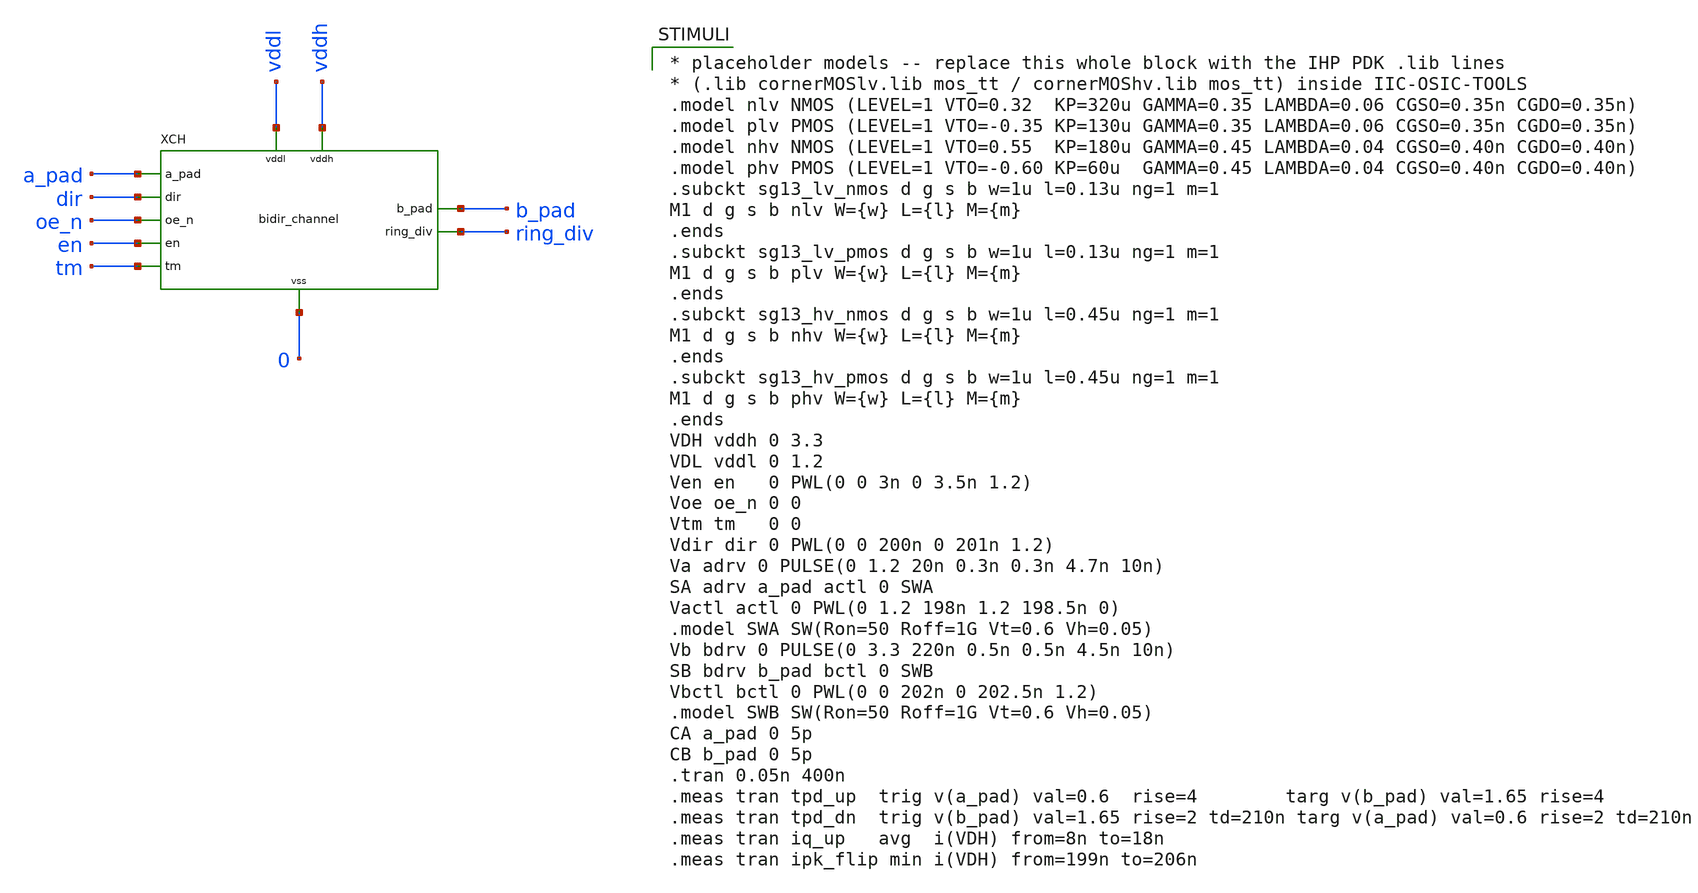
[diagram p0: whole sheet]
** sch_path: xschem/schematics/tb_bidir_channel.sch
**.subckt tb_bidir_channel
XCH a_pad b_pad dir oe_n en tm ring_div vddl vddh 0 bidir_channel
**** begin user architecture code

* placeholder models -- replace this whole block with the IHP PDK .lib lines
* (.lib cornerMOSlv.lib mos_tt / cornerMOShv.lib mos_tt) inside IIC-OSIC-TOOLS
.model nlv NMOS (LEVEL=1 VTO=0.32  KP=320u GAMMA=0.35 LAMBDA=0.06 CGSO=0.35n CGDO=0.35n)
.model plv PMOS (LEVEL=1 VTO=-0.35 KP=130u GAMMA=0.35 LAMBDA=0.06 CGSO=0.35n CGDO=0.35n)
.model nhv NMOS (LEVEL=1 VTO=0.55  KP=180u GAMMA=0.45 LAMBDA=0.04 CGSO=0.40n CGDO=0.40n)
.model phv PMOS (LEVEL=1 VTO=-0.60 KP=60u  GAMMA=0.45 LAMBDA=0.04 CGSO=0.40n CGDO=0.40n)
.subckt sg13_lv_nmos d g s b w=1u l=0.13u ng=1 m=1
M1 d g s b nlv W={w} L={l} M={m}
.ends
.subckt sg13_lv_pmos d g s b w=1u l=0.13u ng=1 m=1
M1 d g s b plv W={w} L={l} M={m}
.ends
.subckt sg13_hv_nmos d g s b w=1u l=0.45u ng=1 m=1
M1 d g s b nhv W={w} L={l} M={m}
.ends
.subckt sg13_hv_pmos d g s b w=1u l=0.45u ng=1 m=1
M1 d g s b phv W={w} L={l} M={m}
.ends
VDH vddh 0 3.3
VDL vddl 0 1.2
Ven en   0 PWL(0 0 3n 0 3.5n 1.2)
Voe oe_n 0 0
Vtm tm   0 0
Vdir dir 0 PWL(0 0 200n 0 201n 1.2)
Va adrv 0 PULSE(0 1.2 20n 0.3n 0.3n 4.7n 10n)
SA adrv a_pad actl 0 SWA
Vactl actl 0 PWL(0 1.2 198n 1.2 198.5n 0)
.model SWA SW(Ron=50 Roff=1G Vt=0.6 Vh=0.05)
Vb bdrv 0 PULSE(0 3.3 220n 0.5n 0.5n 4.5n 10n)
SB bdrv b_pad bctl 0 SWB
Vbctl bctl 0 PWL(0 0 202n 0 202.5n 1.2)
.model SWB SW(Ron=50 Roff=1G Vt=0.6 Vh=0.05)
CA a_pad 0 5p
CB b_pad 0 5p
.tran 0.05n 400n
.meas tran tpd_up  trig v(a_pad) val=0.6  rise=4        targ v(b_pad) val=1.65 rise=4
.meas tran tpd_dn  trig v(b_pad) val=1.65 rise=2 td=210n targ v(a_pad) val=0.6 rise=2 td=210n
.meas tran iq_up   avg  i(VDH) from=8n to=18n
.meas tran ipk_flip min i(VDH) from=199n to=206n

**** end user architecture code
**.ends
.end
